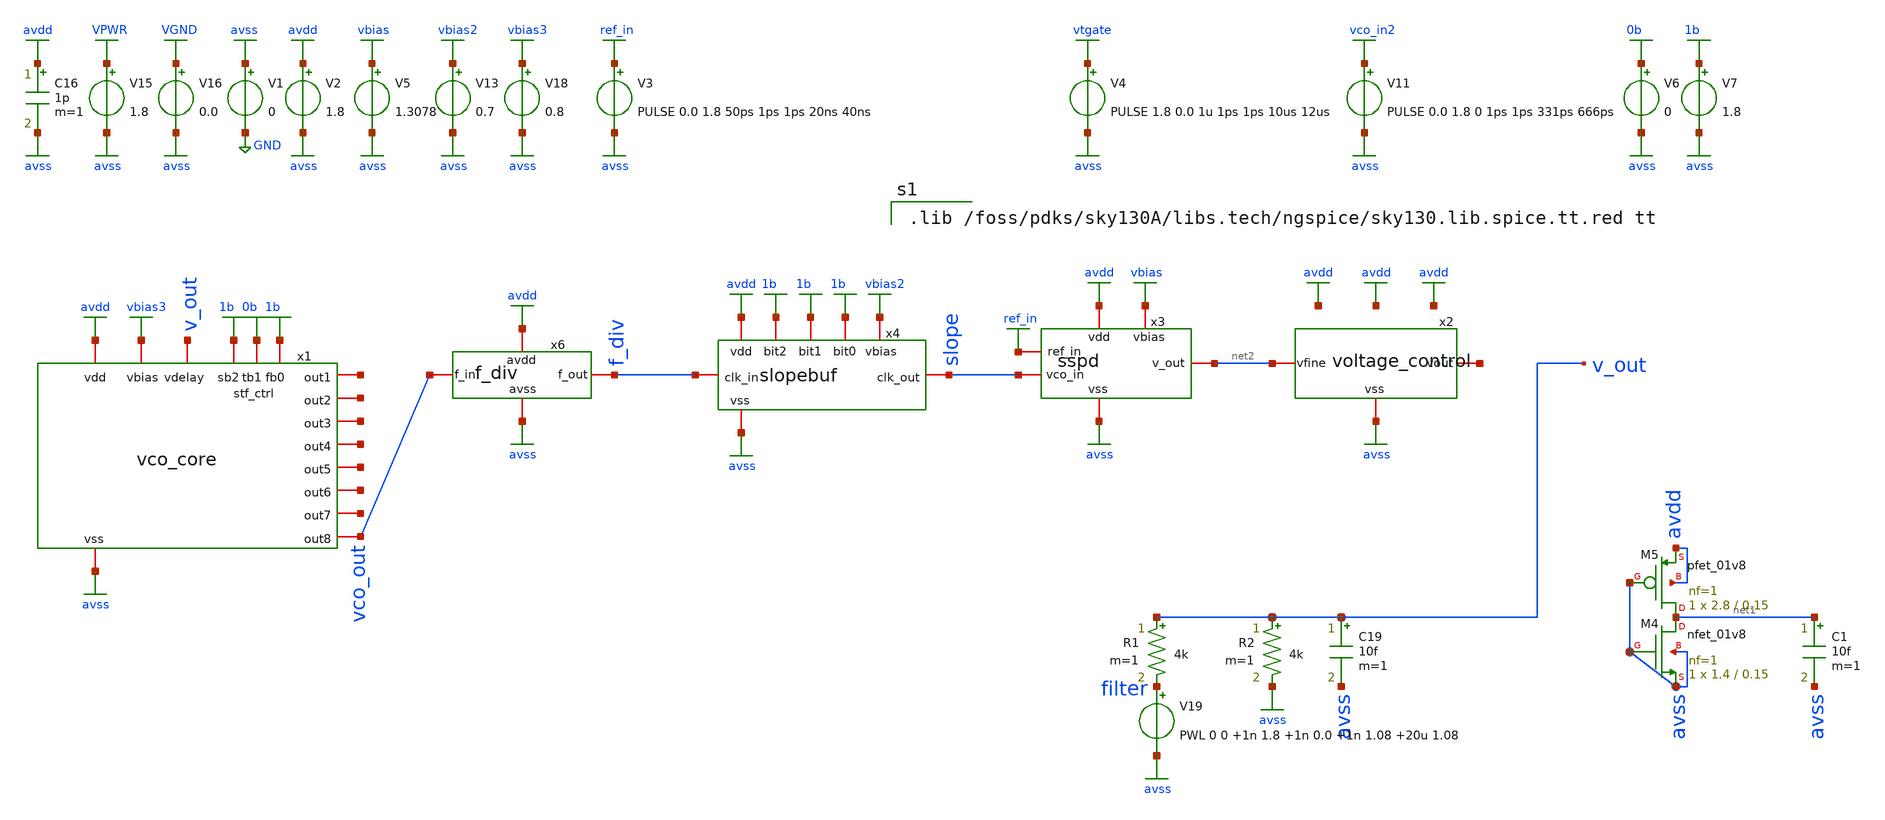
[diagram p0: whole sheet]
** sch_path: xschem/complete_testbench_6.sch
**.subckt complete_testbench_6
V1 avss GND 0
V2 avdd avss 1.8
V3 ref_in avss PULSE 0.0 1.8 50ps 1ps 1ps 20ns 40ns
V5 vbias avss 1.3078
V4 vtgate avss PULSE 1.8 0.0 1u 1ps 1ps 10us 12us
R1 v_out filter 4k m=1
R2 v_out avss 4k m=1
V13 vbias2 avss 0.7
V11 vco_in2 avss PULSE 0.0 1.8 0 1ps 1ps 331ps 666ps
V15 VPWR avss 1.8
V16 VGND avss 0.0
C16 avdd avss 1p m=1
V18 vbias3 avss 0.8
C19 v_out avss 10f m=1
XM4 net1 avss avss avss sky130_fd_pr__nfet_01v8 L=0.15 W=1.4 nf=1 ad='int((nf+1)/2) * W/nf * 0.29' as='int((nf+2)/2) * W/nf * 0.29'
+ pd='2*int((nf+1)/2) * (W/nf + 0.29)' ps='2*int((nf+2)/2) * (W/nf + 0.29)' nrd='0.29 / W' nrs='0.29 / W'
+ sa=0 sb=0 sd=0 mult=1 m=1
XM5 net1 avss avdd avdd sky130_fd_pr__pfet_01v8 L=0.15 W=2.8 nf=1 ad='int((nf+1)/2) * W/nf * 0.29' as='int((nf+2)/2) * W/nf * 0.29'
+ pd='2*int((nf+1)/2) * (W/nf + 0.29)' ps='2*int((nf+2)/2) * (W/nf + 0.29)' nrd='0.29 / W' nrs='0.29 / W'
+ sa=0 sb=0 sd=0 mult=1 m=1
V19 filter avss PWL 0 0 +1n 1.8 +1n 0.0 +1n 1.08 +20u 1.08
x1 avdd net3 avss net4 net5 vbias3 net6 v_out net7 1b 0b net8 net9 1b vco_out vco_core
x2 avss net2 net10 voltage_control
x3 avdd avss ref_in slope vbias net2 sspd
x4 avdd avss f_div slope 1b 1b 1b vbias2 slopebuf
x6 avdd avss vco_out f_div f_div
C1 net1 avss 10f m=1
V6 0b avss 0
V7 1b avss 1.8
**** begin user architecture code

.lib /foss/pdks/sky130A/libs.tech/ngspice/sky130.lib.spice.tt.red tt



.include /foss/pdks/sky130A/libs.ref/sky130_fd_sc_hd/spice/sky130_fd_sc_hd.spice
.control
*save ref_in vco_out f_div slope v_out @V1[i] @V2[i] @V3[i] @V4[i] @V15[i]
save vco_out f_div v_out
tran 0.05n 10000n 5.0n
run
plot vco_out
plot f_div
*plot ref_in slope
plot v_out
*plot @V1[i] @V2[i] @V3[i] @V4[i] @V15[i]
fft ref_in vco_out f_div
plot db(mag(ref_in)) db(mag(f_div)) db(mag(vco_out)) xlimit 0.1meg 4g ylimit 5 -60
*compose values values 10.738n 10.666n 10.596n
*foreach val $&values
*	echo run = $val
*	alter @v4[pulse] = [ 1.8 0.0 0 5ps 5ps 5.323ns $val ] $ vector
*	save ref_in vco_in clk nclk v_out @V1[i] @V3[i] s1 s2
*	tran 0.001n 280n 40n
*	run
*end
*plot tran1.vco_in tran2.vco_in tran3.vco_in
*plot tran1.s2 tran2.s2 tran3.s2
*plot tran1.v_out tran2.v_out tran3.v_out
*plot tran1.v_out
*plot tran2.v_out
*plot tran3.v_out
*plot tran1.s2
*plot tran2.s2
*plot tran3.s2
*compose values start=0.0 stop=1.8 step=0.1
*foreach val $&values
*	echo run = $val
*	alter v5 $val
*	save ref_in vco_in clk nclk v_out @V1[i] @V3[i] s1 s2
*	tran 0.05n 280n 40n
*	run
*end
.endc
.end


**** end user architecture code
**.ends
.GLOBAL avdd
.GLOBAL avss
.GLOBAL GND
.GLOBAL ref_in
.GLOBAL vbias
.GLOBAL vtgate
.GLOBAL vbias2
.GLOBAL vco_in2
.GLOBAL VPWR
.GLOBAL VGND
.GLOBAL vbias3
.GLOBAL 1b
.GLOBAL 0b
.end
